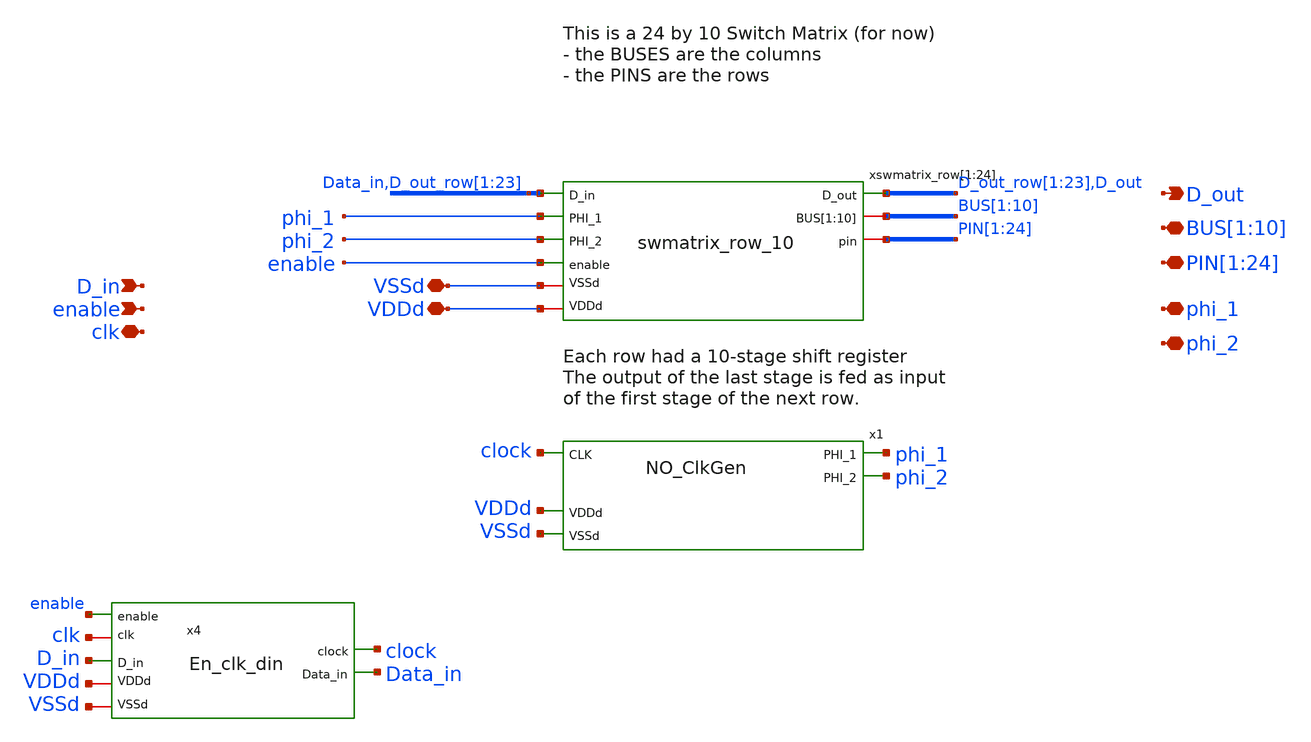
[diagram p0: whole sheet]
** sch_path: swmatrix_24_10/swmatrix_24_by_10_dchain.sch
**.subckt swmatrix_24_by_10_dchain
*+ PIN[1],PIN[2],PIN[3],PIN[4],PIN[5],PIN[6],PIN[7],PIN[8],PIN[9],PIN[10],PIN[11],PIN[12],PIN[13],PIN[14],PIN[15],PIN[16],PIN[17],PIN[18],PIN[19],PIN[20],PIN[21],PIN[22],PIN[23],PIN[24] BUS[1],BUS[2],BUS[3],BUS[4],BUS[5],BUS[6],BUS[7],BUS[8],BUS[9],BUS[10] D_in D_out VDDd VSSd enable
*+ clk phi_2 phi_1
*.iopin
*+ PIN[1],PIN[2],PIN[3],PIN[4],PIN[5],PIN[6],PIN[7],PIN[8],PIN[9],PIN[10],PIN[11],PIN[12],PIN[13],PIN[14],PIN[15],PIN[16],PIN[17],PIN[18],PIN[19],PIN[20],PIN[21],PIN[22],PIN[23],PIN[24]
*.iopin BUS[1],BUS[2],BUS[3],BUS[4],BUS[5],BUS[6],BUS[7],BUS[8],BUS[9],BUS[10]
*.ipin D_in
*.opin D_out
*.iopin VDDd
*.iopin VSSd
*.ipin enable
*.iopin clk
*.iopin phi_2
*.iopin phi_1
xswmatrix_row[1] D_out_row[1] Data_in phi_1 phi_2 enable BUS[1] BUS[2] BUS[3] BUS[4] BUS[5] BUS[6]
+ BUS[7] BUS[8] BUS[9] BUS[10] VDDd PIN[1] VSSd swmatrix_row_10
xswmatrix_row[2] D_out_row[2] D_out_row[1] phi_1 phi_2 enable BUS[1] BUS[2] BUS[3] BUS[4] BUS[5]
+ BUS[6] BUS[7] BUS[8] BUS[9] BUS[10] VDDd PIN[2] VSSd swmatrix_row_10
xswmatrix_row[3] D_out_row[3] D_out_row[2] phi_1 phi_2 enable BUS[1] BUS[2] BUS[3] BUS[4] BUS[5]
+ BUS[6] BUS[7] BUS[8] BUS[9] BUS[10] VDDd PIN[3] VSSd swmatrix_row_10
xswmatrix_row[4] D_out_row[4] D_out_row[3] phi_1 phi_2 enable BUS[1] BUS[2] BUS[3] BUS[4] BUS[5]
+ BUS[6] BUS[7] BUS[8] BUS[9] BUS[10] VDDd PIN[4] VSSd swmatrix_row_10
xswmatrix_row[5] D_out_row[5] D_out_row[4] phi_1 phi_2 enable BUS[1] BUS[2] BUS[3] BUS[4] BUS[5]
+ BUS[6] BUS[7] BUS[8] BUS[9] BUS[10] VDDd PIN[5] VSSd swmatrix_row_10
xswmatrix_row[6] D_out_row[6] D_out_row[5] phi_1 phi_2 enable BUS[1] BUS[2] BUS[3] BUS[4] BUS[5]
+ BUS[6] BUS[7] BUS[8] BUS[9] BUS[10] VDDd PIN[6] VSSd swmatrix_row_10
xswmatrix_row[7] D_out_row[7] D_out_row[6] phi_1 phi_2 enable BUS[1] BUS[2] BUS[3] BUS[4] BUS[5]
+ BUS[6] BUS[7] BUS[8] BUS[9] BUS[10] VDDd PIN[7] VSSd swmatrix_row_10
xswmatrix_row[8] D_out_row[8] D_out_row[7] phi_1 phi_2 enable BUS[1] BUS[2] BUS[3] BUS[4] BUS[5]
+ BUS[6] BUS[7] BUS[8] BUS[9] BUS[10] VDDd PIN[8] VSSd swmatrix_row_10
xswmatrix_row[9] D_out_row[9] D_out_row[8] phi_1 phi_2 enable BUS[1] BUS[2] BUS[3] BUS[4] BUS[5]
+ BUS[6] BUS[7] BUS[8] BUS[9] BUS[10] VDDd PIN[9] VSSd swmatrix_row_10
xswmatrix_row[10] D_out_row[10] D_out_row[9] phi_1 phi_2 enable BUS[1] BUS[2] BUS[3] BUS[4] BUS[5]
+ BUS[6] BUS[7] BUS[8] BUS[9] BUS[10] VDDd PIN[10] VSSd swmatrix_row_10
xswmatrix_row[11] D_out_row[11] D_out_row[10] phi_1 phi_2 enable BUS[1] BUS[2] BUS[3] BUS[4] BUS[5]
+ BUS[6] BUS[7] BUS[8] BUS[9] BUS[10] VDDd PIN[11] VSSd swmatrix_row_10
xswmatrix_row[12] D_out_row[12] D_out_row[11] phi_1 phi_2 enable BUS[1] BUS[2] BUS[3] BUS[4] BUS[5]
+ BUS[6] BUS[7] BUS[8] BUS[9] BUS[10] VDDd PIN[12] VSSd swmatrix_row_10
xswmatrix_row[13] D_out_row[13] D_out_row[12] phi_1 phi_2 enable BUS[1] BUS[2] BUS[3] BUS[4] BUS[5]
+ BUS[6] BUS[7] BUS[8] BUS[9] BUS[10] VDDd PIN[13] VSSd swmatrix_row_10
xswmatrix_row[14] D_out_row[14] D_out_row[13] phi_1 phi_2 enable BUS[1] BUS[2] BUS[3] BUS[4] BUS[5]
+ BUS[6] BUS[7] BUS[8] BUS[9] BUS[10] VDDd PIN[14] VSSd swmatrix_row_10
xswmatrix_row[15] D_out_row[15] D_out_row[14] phi_1 phi_2 enable BUS[1] BUS[2] BUS[3] BUS[4] BUS[5]
+ BUS[6] BUS[7] BUS[8] BUS[9] BUS[10] VDDd PIN[15] VSSd swmatrix_row_10
xswmatrix_row[16] D_out_row[16] D_out_row[15] phi_1 phi_2 enable BUS[1] BUS[2] BUS[3] BUS[4] BUS[5]
+ BUS[6] BUS[7] BUS[8] BUS[9] BUS[10] VDDd PIN[16] VSSd swmatrix_row_10
xswmatrix_row[17] D_out_row[17] D_out_row[16] phi_1 phi_2 enable BUS[1] BUS[2] BUS[3] BUS[4] BUS[5]
+ BUS[6] BUS[7] BUS[8] BUS[9] BUS[10] VDDd PIN[17] VSSd swmatrix_row_10
xswmatrix_row[18] D_out_row[18] D_out_row[17] phi_1 phi_2 enable BUS[1] BUS[2] BUS[3] BUS[4] BUS[5]
+ BUS[6] BUS[7] BUS[8] BUS[9] BUS[10] VDDd PIN[18] VSSd swmatrix_row_10
xswmatrix_row[19] D_out_row[19] D_out_row[18] phi_1 phi_2 enable BUS[1] BUS[2] BUS[3] BUS[4] BUS[5]
+ BUS[6] BUS[7] BUS[8] BUS[9] BUS[10] VDDd PIN[19] VSSd swmatrix_row_10
xswmatrix_row[20] D_out_row[20] D_out_row[19] phi_1 phi_2 enable BUS[1] BUS[2] BUS[3] BUS[4] BUS[5]
+ BUS[6] BUS[7] BUS[8] BUS[9] BUS[10] VDDd PIN[20] VSSd swmatrix_row_10
xswmatrix_row[21] D_out_row[21] D_out_row[20] phi_1 phi_2 enable BUS[1] BUS[2] BUS[3] BUS[4] BUS[5]
+ BUS[6] BUS[7] BUS[8] BUS[9] BUS[10] VDDd PIN[21] VSSd swmatrix_row_10
xswmatrix_row[22] D_out_row[22] D_out_row[21] phi_1 phi_2 enable BUS[1] BUS[2] BUS[3] BUS[4] BUS[5]
+ BUS[6] BUS[7] BUS[8] BUS[9] BUS[10] VDDd PIN[22] VSSd swmatrix_row_10
xswmatrix_row[23] D_out_row[23] D_out_row[22] phi_1 phi_2 enable BUS[1] BUS[2] BUS[3] BUS[4] BUS[5]
+ BUS[6] BUS[7] BUS[8] BUS[9] BUS[10] VDDd PIN[23] VSSd swmatrix_row_10
xswmatrix_row[24] D_out D_out_row[23] phi_1 phi_2 enable BUS[1] BUS[2] BUS[3] BUS[4] BUS[5] BUS[6]
+ BUS[7] BUS[8] BUS[9] BUS[10] VDDd PIN[24] VSSd swmatrix_row_10
x1 phi_2 clock phi_1 VDDd VSSd NO_ClkGen
x4 VDDd VSSd clk clock enable D_in Data_in En_clk_din
**.ends
.end
